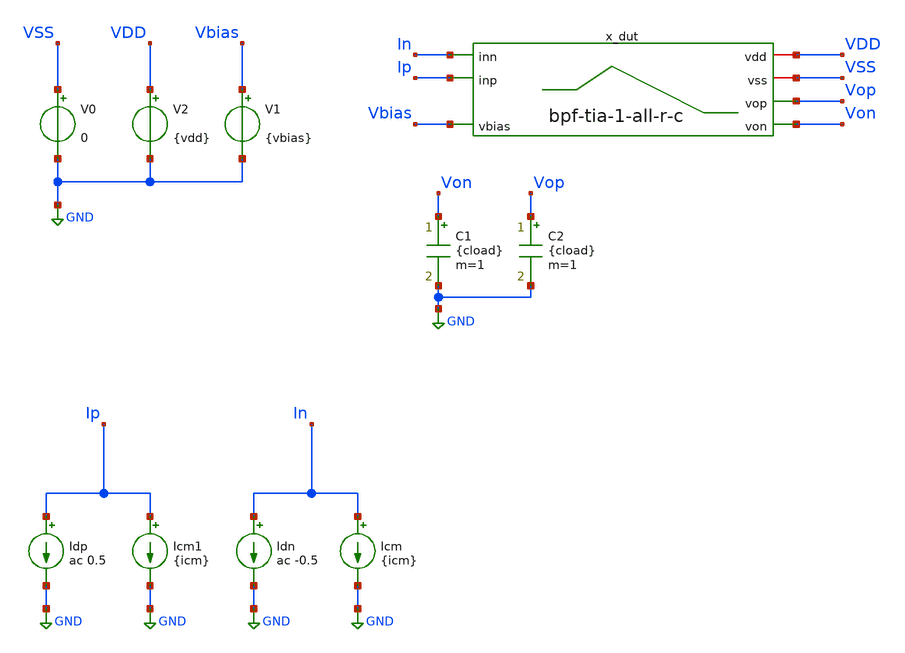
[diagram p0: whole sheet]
** sch_path: examples/tunable-tia/gf180/tia-bpf-1/tb_ac.sch
**.subckt tb_ac
V0 VSS GND 0
V2 VDD GND {vdd}
x_dut VDD VSS Vop Von In Ip Vbias bpf-tia-1-all-r-c
V1 Vbias GND {vbias}
C1 Von GND {cload} m=1
C2 Vop GND {cload} m=1
Icm In GND {icm}
Idn In GND ac -0.5
Icm1 Ip GND {icm}
Idp Ip GND ac 0.5
**** begin user architecture code


.control

    echo ==================================
    echo start of Control
    echo ==================================

    save all

    echo
    echo (A) start of OP
    echo ----------------------------------

    * operating point
    op
    let gm_id = @m.x_dut.xm1.m0[gm]/@m.x_dut.xm1.m0[id]
    print all
    write op.raw

    echo ----------------------------------
    echo END of OP
    echo ----------------------------------

    set appendwrite

    echo
    echo (B) start of AC Sim
    echo ----------------------------------

    * run ac simulation
    ac dec 200 1e5 1e12

    echo (1) post processing the AC sim
    * magnitude
    let Vout = v(Vop) - v(Von)
    let vout_mag = abs(v(Vout))
    let vout_mag_db = 20*log(vout_mag)/log(10)

    * raw phase (between -180 and 180)
    let vout_phase = phase(v(Vout)) * 180/pi

    echo (2) measuring A0, PM, UGF...

    * Bandpass response parameters
    meas ac GMAX max vout_mag
    meas ac FC when vout_mag=GMAX

    let gmax_3db = GMAX/sqrt(2)

    meas ac FLO when vout_mag=gmax_3db cross=1
    meas ac FHI when vout_mag=gmax_3db cross=2

    let BW = FHI-FLO
    let Q  = FC/BW
    let gain_db = 20 * log(GMAX) / log(10)
    print BW Q gain_db
    *meas ac A0 find vout_mag at=1k
    meas ac PM find vout_phase when vout_mag=1
    meas ac UGF when vout_mag=1 fall=1

    echo (3) plotting...
    plot vout_mag

    echo ----------------------------------
    echo END of AC sim
    echo  ----------------------------------

    echo SAVING SIMULATION RESULTS IN THE RAW FILE
    save all
    write

    echo ==================================
    echo END of Control
    echo ==================================
.endc



.include $::180MCU_MODELS/design.ngspice
.lib $::180MCU_MODELS/sm141064.ngspice typical

.lib $::180MCU_MODELS/sm141064.ngspice res_typical
* .lib $::180MCU_MODELS/sm141064.ngspice res_statistical




*.option savecurrents
* Saving gm values for transistors
.save @m.x_dut.xm1.m0[gm]
.save @m.x_dut.xm2.m0[gm]

* Saving id values for transistors
.save @m.x_dut.xm1.m0[id]
.save @m.x_dut.xm2.m0[id]





* TB Parameters
.param idd=1.8e-6
.param icm=0.5e-6
.param vdd=6.0
.param vbias=1.0
.param cload=1p





* All DUT parameters

* MOSFET PARAMETERS
.param x_dut_m1_2_w=0.22u
.param x_dut_m1_2_l=0.40u
.param x_dut_m1_2_nf=2

* PASSIVE ELEMENT PARAMETERS
.param x_dut_ldd=2n
.param x_dut_cdd=1n

.param x_dut_rs=1k

.param x_dut_r4=1k


**** end user architecture code
**.ends

* expanding   symbol:  tia-bpf-1/bpf-tia-1-all-r-c.sym # of pins=7
** sym_path: examples/tunable-tia/gf180/tia-bpf-1/bpf-tia-1-all-r-c.sym
** sch_path: examples/tunable-tia/gf180/tia-bpf-1/bpf-tia-1-all-r-c.sch
.subckt bpf-tia-1-all-r-c vdd vss vop von inn inp vbias
*.iopin vdd
*.iopin vss
*.ipin inp
*.ipin inn
*.opin von
*.opin vop
*.ipin vbias
XM1 von vbias inp vss nfet_03v3 L={x_dut_m1_2_l} W={x_dut_m1_2_w} nf=2 ad='int((nf+1)/2) * W/nf * 0.18u'
+ as='int((nf+2)/2) * W/nf * 0.18u' pd='2*int((nf+1)/2) * (W/nf + 0.18u)' ps='2*int((nf+2)/2) * (W/nf + 0.18u)'
+ nrd='0.18u / W' nrs='0.18u / W' sa=0 sb=0 sd=0 m=1
XM2 vop vbias inn vss nfet_03v3 L={x_dut_m1_2_l} W={x_dut_m1_2_w} nf=2 ad='int((nf+1)/2) * W/nf * 0.18u'
+ as='int((nf+2)/2) * W/nf * 0.18u' pd='2*int((nf+1)/2) * (W/nf + 0.18u)' ps='2*int((nf+2)/2) * (W/nf + 0.18u)'
+ nrd='0.18u / W' nrs='0.18u / W' sa=0 sb=0 sd=0 m=1
R1 inp vss {x_dut_rs} m=1
R2 inn vss {x_dut_rs} m=1
C1 vdd von {x_dut_cdd} m=1
C2 vdd vop {x_dut_cdd} m=1
L2 vdd von {x_dut_ldd} m=1
L3 vdd vop {x_dut_ldd} m=1
R4 von vop {x_dut_r4} m=1
.ends

.GLOBAL GND
.end
